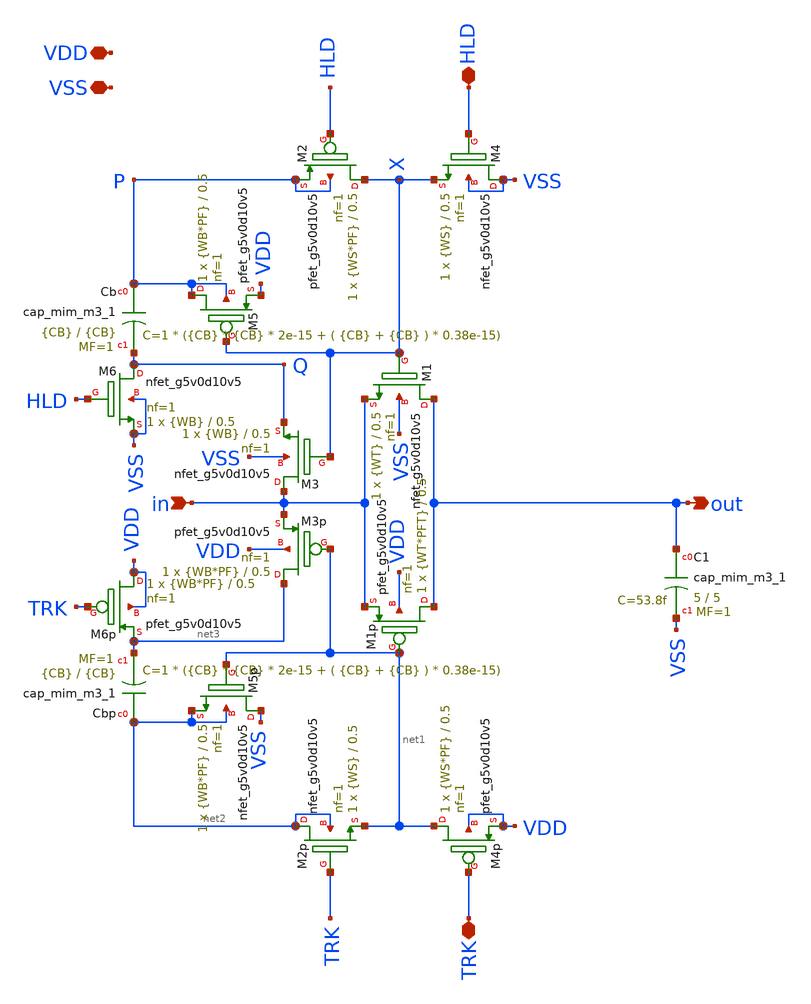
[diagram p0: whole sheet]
** sch_path: xschem/parametric_track_and_hold.sch
**.subckt parametric_track_and_hold VSS VDD in out TRK HLD
*.iopin VSS
*.iopin VDD
*.ipin in
*.opin out
*.iopin TRK
*.iopin HLD
XC1 out VSS sky130_fd_pr__cap_mim_m3_1 W=5 L=5 MF=1 m=1
XM1 out X in VSS sky130_fd_pr__nfet_g5v0d10v5 L=0.5 W={WT} nf=1 ad='int((nf+1)/2) * W/nf * 0.29' as='int((nf+2)/2) * W/nf * 0.29'
+ pd='2*int((nf+1)/2) * (W/nf + 0.29)' ps='2*int((nf+2)/2) * (W/nf + 0.29)' nrd='0.29 / W' nrs='0.29 / W'
+ sa=0 sb=0 sd=0 mult=1 m=1
XM1p out net1 in VDD sky130_fd_pr__pfet_g5v0d10v5 L=0.5 W={WT*PFT} nf=1 ad='int((nf+1)/2) * W/nf * 0.29'
+ as='int((nf+2)/2) * W/nf * 0.29' pd='2*int((nf+1)/2) * (W/nf + 0.29)' ps='2*int((nf+2)/2) * (W/nf + 0.29)'
+ nrd='0.29 / W' nrs='0.29 / W' sa=0 sb=0 sd=0 mult=1 m=1
XM4 VSS HLD X VSS sky130_fd_pr__nfet_g5v0d10v5 L=0.5 W={WS} nf=1 ad='int((nf+1)/2) * W/nf * 0.29' as='int((nf+2)/2) * W/nf * 0.29'
+ pd='2*int((nf+1)/2) * (W/nf + 0.29)' ps='2*int((nf+2)/2) * (W/nf + 0.29)' nrd='0.29 / W' nrs='0.29 / W'
+ sa=0 sb=0 sd=0 mult=1 m=1
XM4p net1 TRK VDD VDD sky130_fd_pr__pfet_g5v0d10v5 L=0.5 W={WS*PF} nf=1 ad='int((nf+1)/2) * W/nf * 0.29'
+ as='int((nf+2)/2) * W/nf * 0.29' pd='2*int((nf+1)/2) * (W/nf + 0.29)' ps='2*int((nf+2)/2) * (W/nf + 0.29)'
+ nrd='0.29 / W' nrs='0.29 / W' sa=0 sb=0 sd=0 mult=1 m=1
XM2 X HLD P P sky130_fd_pr__pfet_g5v0d10v5 L=0.5 W={WS*PF} nf=1 ad='int((nf+1)/2) * W/nf * 0.29' as='int((nf+2)/2) * W/nf * 0.29'
+ pd='2*int((nf+1)/2) * (W/nf + 0.29)' ps='2*int((nf+2)/2) * (W/nf + 0.29)' nrd='0.29 / W' nrs='0.29 / W'
+ sa=0 sb=0 sd=0 mult=1 m=1
XM2p net2 TRK net1 net2 sky130_fd_pr__nfet_g5v0d10v5 L=0.5 W={WS} nf=1 ad='int((nf+1)/2) * W/nf * 0.29'
+ as='int((nf+2)/2) * W/nf * 0.29' pd='2*int((nf+1)/2) * (W/nf + 0.29)' ps='2*int((nf+2)/2) * (W/nf + 0.29)'
+ nrd='0.29 / W' nrs='0.29 / W' sa=0 sb=0 sd=0 mult=1 m=1
XM3 in X Q VSS sky130_fd_pr__nfet_g5v0d10v5 L=0.5 W={WB} nf=1 ad='int((nf+1)/2) * W/nf * 0.29' as='int((nf+2)/2) * W/nf * 0.29'
+ pd='2*int((nf+1)/2) * (W/nf + 0.29)' ps='2*int((nf+2)/2) * (W/nf + 0.29)' nrd='0.29 / W' nrs='0.29 / W'
+ sa=0 sb=0 sd=0 mult=1 m=1
XM6 Q HLD VSS VSS sky130_fd_pr__nfet_g5v0d10v5 L=0.5 W={WB} nf=1 ad='int((nf+1)/2) * W/nf * 0.29' as='int((nf+2)/2) * W/nf * 0.29'
+ pd='2*int((nf+1)/2) * (W/nf + 0.29)' ps='2*int((nf+2)/2) * (W/nf + 0.29)' nrd='0.29 / W' nrs='0.29 / W'
+ sa=0 sb=0 sd=0 mult=1 m=1
XM3p net3 net1 in VDD sky130_fd_pr__pfet_g5v0d10v5 L=0.5 W={WB*PF} nf=1 ad='int((nf+1)/2) * W/nf * 0.29'
+ as='int((nf+2)/2) * W/nf * 0.29' pd='2*int((nf+1)/2) * (W/nf + 0.29)' ps='2*int((nf+2)/2) * (W/nf + 0.29)'
+ nrd='0.29 / W' nrs='0.29 / W' sa=0 sb=0 sd=0 mult=1 m=1
XM6p VDD TRK net3 VDD sky130_fd_pr__pfet_g5v0d10v5 L=0.5 W={WB*PF} nf=1 ad='int((nf+1)/2) * W/nf * 0.29'
+ as='int((nf+2)/2) * W/nf * 0.29' pd='2*int((nf+1)/2) * (W/nf + 0.29)' ps='2*int((nf+2)/2) * (W/nf + 0.29)'
+ nrd='0.29 / W' nrs='0.29 / W' sa=0 sb=0 sd=0 mult=1 m=1
XM5 P X VDD P sky130_fd_pr__pfet_g5v0d10v5 L=0.5 W={WB*PF} nf=1 ad='int((nf+1)/2) * W/nf * 0.29' as='int((nf+2)/2) * W/nf * 0.29'
+ pd='2*int((nf+1)/2) * (W/nf + 0.29)' ps='2*int((nf+2)/2) * (W/nf + 0.29)' nrd='0.29 / W' nrs='0.29 / W'
+ sa=0 sb=0 sd=0 mult=1 m=1
XCb P Q sky130_fd_pr__cap_mim_m3_1 W={CB} L={CB} MF=1 m=1
XCbp net2 net3 sky130_fd_pr__cap_mim_m3_1 W={CB} L={CB} MF=1 m=1
XM5p VSS net1 net2 net2 sky130_fd_pr__nfet_g5v0d10v5 L=0.5 W={WB*PF} nf=1 ad='int((nf+1)/2) * W/nf * 0.29'
+ as='int((nf+2)/2) * W/nf * 0.29' pd='2*int((nf+1)/2) * (W/nf + 0.29)' ps='2*int((nf+2)/2) * (W/nf + 0.29)'
+ nrd='0.29 / W' nrs='0.29 / W' sa=0 sb=0 sd=0 mult=1 m=1
**.ends
.end
